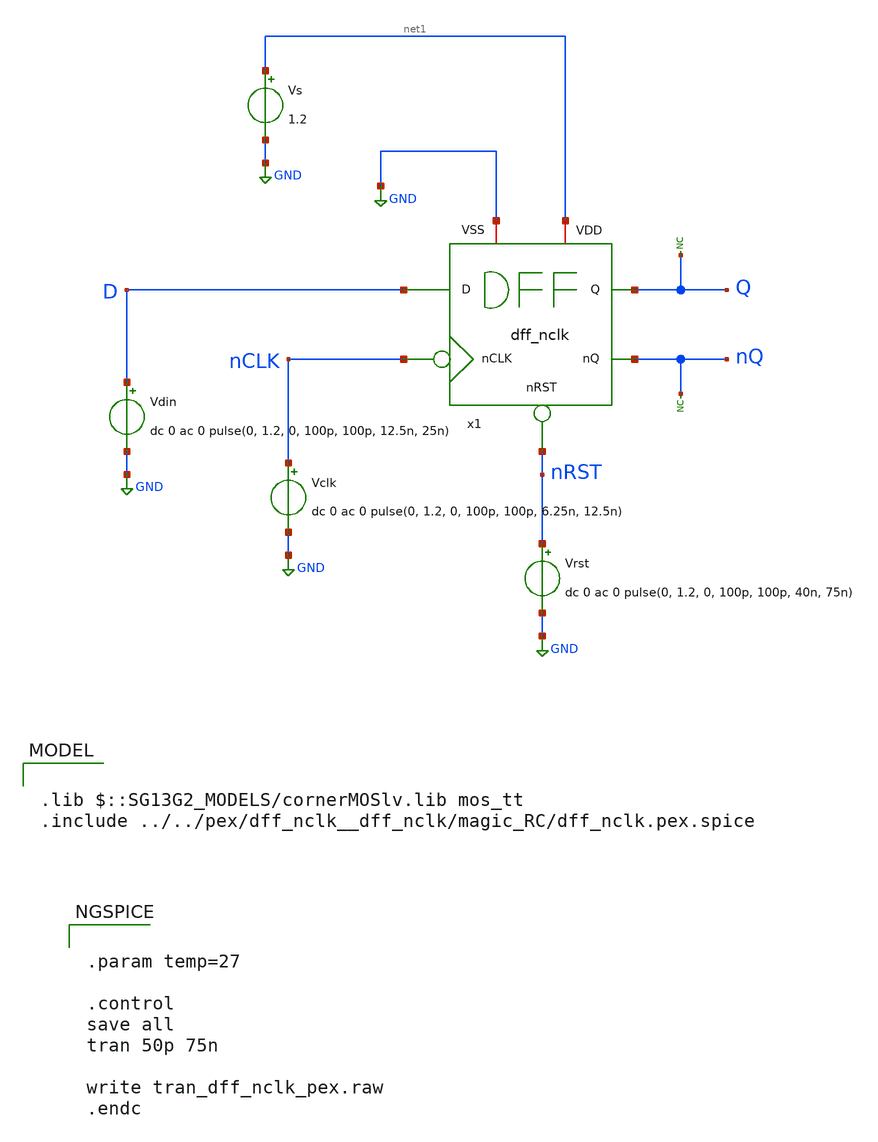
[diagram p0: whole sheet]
** sch_path: Combined_Design/design_data/xschem/dff_nclk_pex_tb.sch

.lib $::SG13G2_MODELS/cornerMOSlv.lib mos_tt
.include ../../pex/dff_nclk__dff_nclk/magic_RC/dff_nclk.pex.spice

**.subckt dff_nclk_pex_tb
Vdin D GND dc 0 ac 0 pulse(0, 1.2, 0, 100p, 100p, 12.5n, 25n)
Vclk nCLK GND dc 0 ac 0 pulse(0, 1.2, 0, 100p, 100p, 6.25n, 12.5n)
Vrst nRST GND dc 0 ac 0 pulse(0, 1.2, 0, 100p, 100p, 40n, 75n)
* noconn nQ
* noconn Q
x1 nCLK Q D nQ nRST net1 GND dff_nclk
Vs net1 GND 1.2
**** begin user architecture code


.param temp=27

.control
save all
tran 50p 75n

write tran_dff_nclk_pex.raw
.endc


**** end user architecture code
**.ends
.GLOBAL GND
.end
